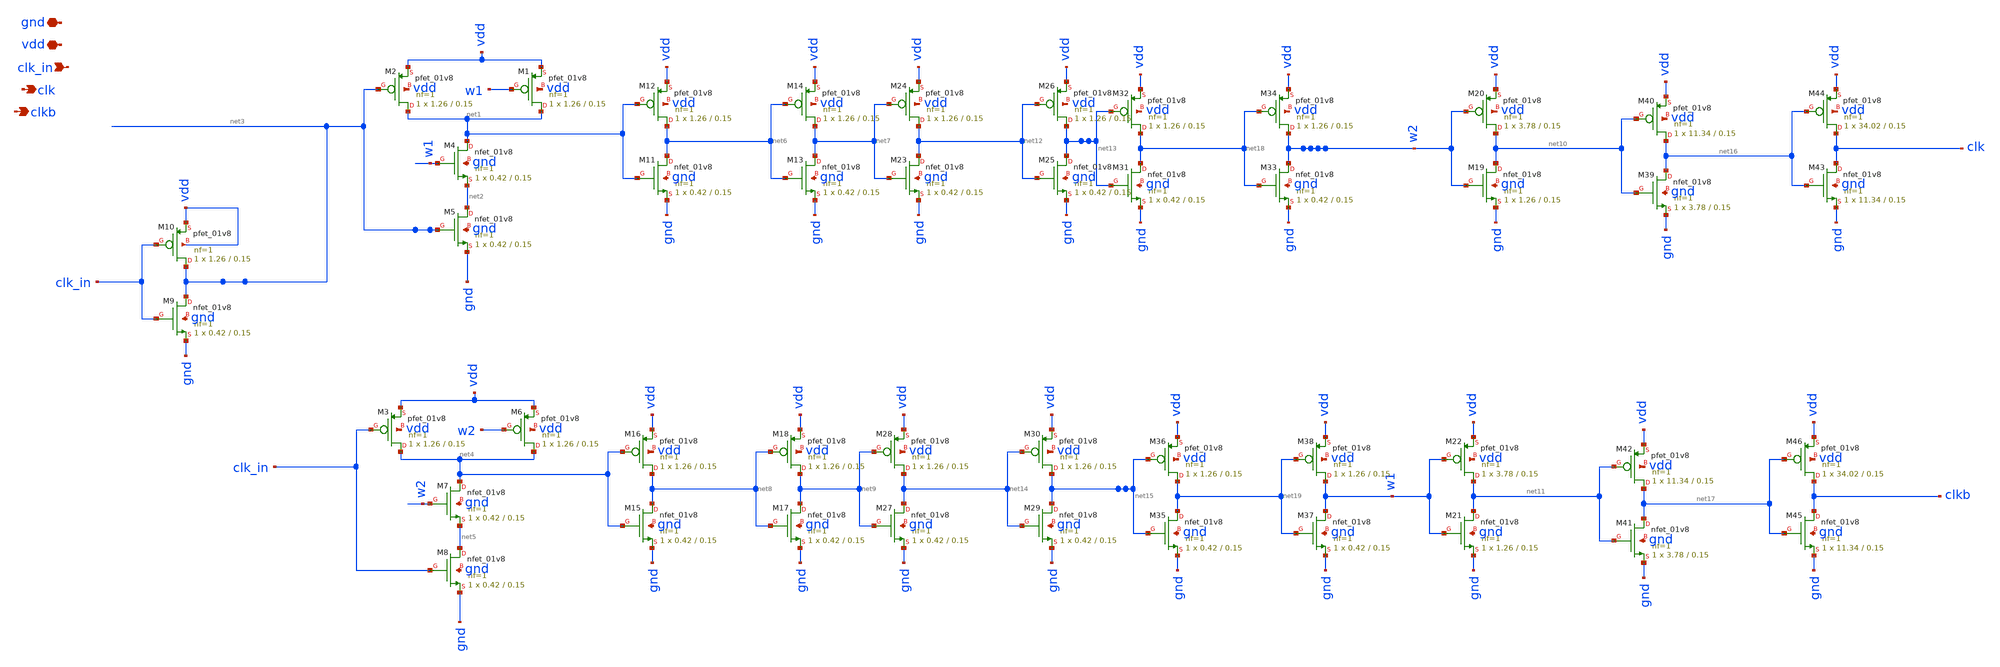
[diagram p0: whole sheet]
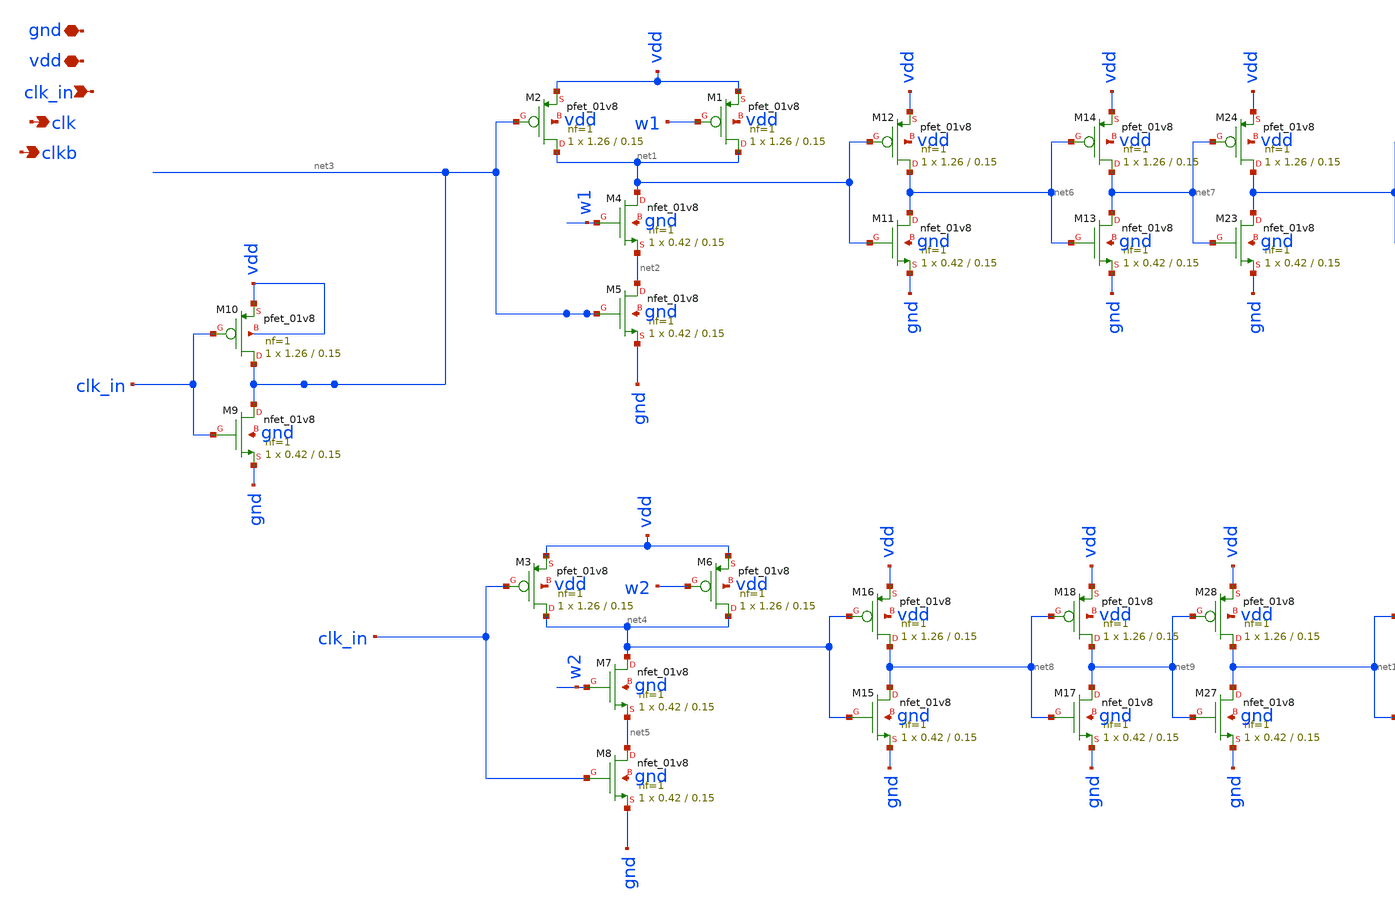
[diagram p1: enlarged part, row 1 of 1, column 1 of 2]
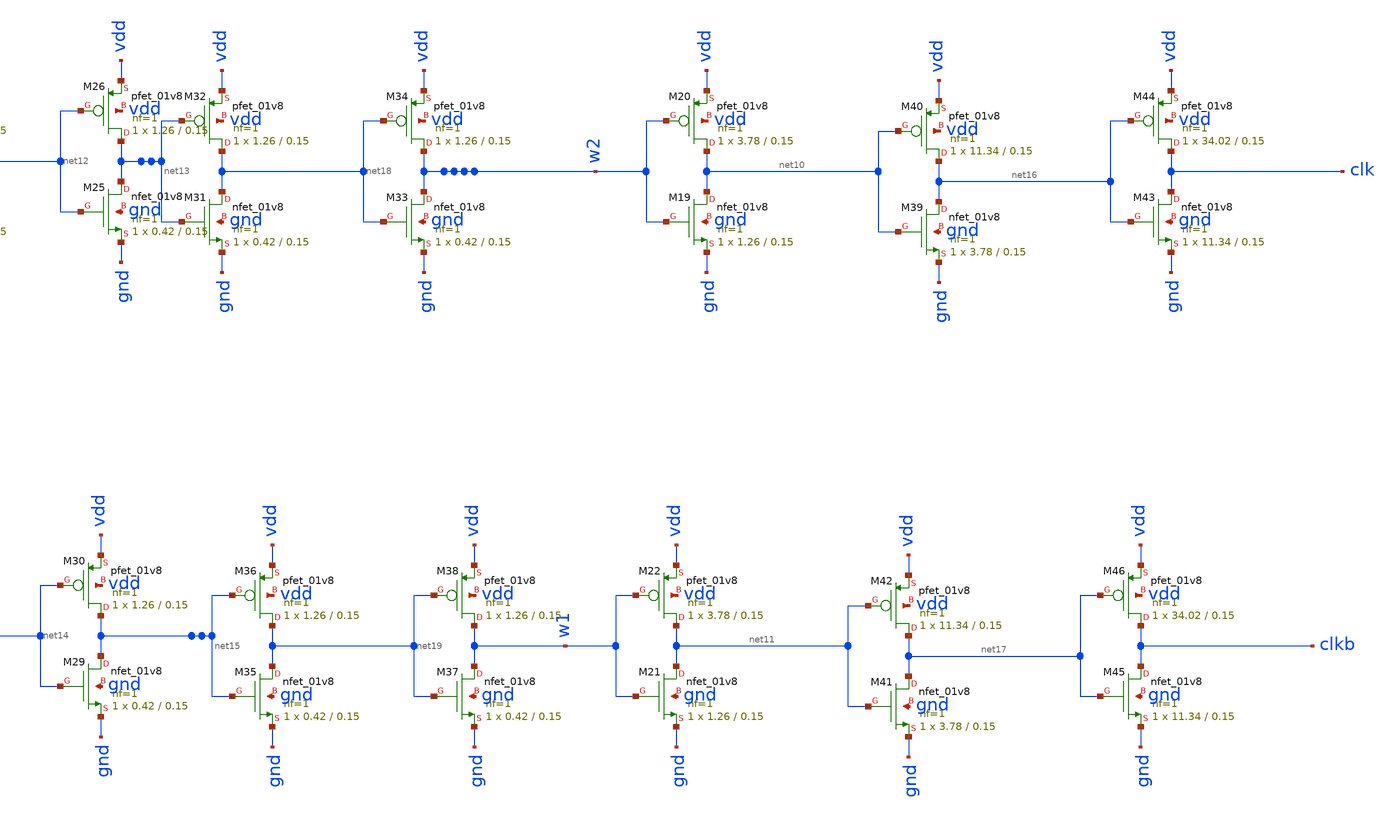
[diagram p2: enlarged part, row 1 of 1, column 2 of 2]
** sch_path: xschem/charge_pumps2/clock_1.sch
**.subckt clock_1 clk_in vdd gnd clk clkb
*.ipin clk_in
*.iopin vdd
*.iopin gnd
*.opin clk
*.opin clkb
XM2 net1 net3 vdd vdd sky130_fd_pr__pfet_01v8 L=0.15 W=1.26 nf=1 ad='int((nf+1)/2) * W/nf * 0.29' as='int((nf+2)/2) * W/nf * 0.29'
+ pd='2*int((nf+1)/2) * (W/nf + 0.29)' ps='2*int((nf+2)/2) * (W/nf + 0.29)' nrd='0.29 / W' nrs='0.29 / W'
+ sa=0 sb=0 sd=0 mult=1 m=1
XM1 net1 w1 vdd vdd sky130_fd_pr__pfet_01v8 L=0.15 W=1.26 nf=1 ad='int((nf+1)/2) * W/nf * 0.29' as='int((nf+2)/2) * W/nf * 0.29'
+ pd='2*int((nf+1)/2) * (W/nf + 0.29)' ps='2*int((nf+2)/2) * (W/nf + 0.29)' nrd='0.29 / W' nrs='0.29 / W'
+ sa=0 sb=0 sd=0 mult=1 m=1
XM4 net1 w1 net2 gnd sky130_fd_pr__nfet_01v8 L=0.15 W=0.42 nf=1 ad='int((nf+1)/2) * W/nf * 0.29' as='int((nf+2)/2) * W/nf * 0.29'
+ pd='2*int((nf+1)/2) * (W/nf + 0.29)' ps='2*int((nf+2)/2) * (W/nf + 0.29)' nrd='0.29 / W' nrs='0.29 / W'
+ sa=0 sb=0 sd=0 mult=1 m=1
XM5 net2 net3 gnd gnd sky130_fd_pr__nfet_01v8 L=0.15 W=0.42 nf=1 ad='int((nf+1)/2) * W/nf * 0.29' as='int((nf+2)/2) * W/nf * 0.29'
+ pd='2*int((nf+1)/2) * (W/nf + 0.29)' ps='2*int((nf+2)/2) * (W/nf + 0.29)' nrd='0.29 / W' nrs='0.29 / W'
+ sa=0 sb=0 sd=0 mult=1 m=1
XM3 net4 clk_in vdd vdd sky130_fd_pr__pfet_01v8 L=0.15 W=1.26 nf=1 ad='int((nf+1)/2) * W/nf * 0.29' as='int((nf+2)/2) * W/nf * 0.29'
+ pd='2*int((nf+1)/2) * (W/nf + 0.29)' ps='2*int((nf+2)/2) * (W/nf + 0.29)' nrd='0.29 / W' nrs='0.29 / W'
+ sa=0 sb=0 sd=0 mult=1 m=1
XM6 net4 w2 vdd vdd sky130_fd_pr__pfet_01v8 L=0.15 W=1.26 nf=1 ad='int((nf+1)/2) * W/nf * 0.29' as='int((nf+2)/2) * W/nf * 0.29'
+ pd='2*int((nf+1)/2) * (W/nf + 0.29)' ps='2*int((nf+2)/2) * (W/nf + 0.29)' nrd='0.29 / W' nrs='0.29 / W'
+ sa=0 sb=0 sd=0 mult=1 m=1
XM7 net4 w2 net5 gnd sky130_fd_pr__nfet_01v8 L=0.15 W=0.42 nf=1 ad='int((nf+1)/2) * W/nf * 0.29' as='int((nf+2)/2) * W/nf * 0.29'
+ pd='2*int((nf+1)/2) * (W/nf + 0.29)' ps='2*int((nf+2)/2) * (W/nf + 0.29)' nrd='0.29 / W' nrs='0.29 / W'
+ sa=0 sb=0 sd=0 mult=1 m=1
XM8 net5 clk_in gnd gnd sky130_fd_pr__nfet_01v8 L=0.15 W=0.42 nf=1 ad='int((nf+1)/2) * W/nf * 0.29' as='int((nf+2)/2) * W/nf * 0.29'
+ pd='2*int((nf+1)/2) * (W/nf + 0.29)' ps='2*int((nf+2)/2) * (W/nf + 0.29)' nrd='0.29 / W' nrs='0.29 / W'
+ sa=0 sb=0 sd=0 mult=1 m=1
XM9 net3 clk_in gnd gnd sky130_fd_pr__nfet_01v8 L=0.15 W=0.42 nf=1 ad='int((nf+1)/2) * W/nf * 0.29' as='int((nf+2)/2) * W/nf * 0.29'
+ pd='2*int((nf+1)/2) * (W/nf + 0.29)' ps='2*int((nf+2)/2) * (W/nf + 0.29)' nrd='0.29 / W' nrs='0.29 / W'
+ sa=0 sb=0 sd=0 mult=1 m=1
XM10 net3 clk_in vdd vdd sky130_fd_pr__pfet_01v8 L=0.15 W=1.26 nf=1 ad='int((nf+1)/2) * W/nf * 0.29'
+ as='int((nf+2)/2) * W/nf * 0.29' pd='2*int((nf+1)/2) * (W/nf + 0.29)' ps='2*int((nf+2)/2) * (W/nf + 0.29)'
+ nrd='0.29 / W' nrs='0.29 / W' sa=0 sb=0 sd=0 mult=1 m=1
XM11 net6 net1 gnd gnd sky130_fd_pr__nfet_01v8 L=0.15 W=0.42 nf=1 ad='int((nf+1)/2) * W/nf * 0.29' as='int((nf+2)/2) * W/nf * 0.29'
+ pd='2*int((nf+1)/2) * (W/nf + 0.29)' ps='2*int((nf+2)/2) * (W/nf + 0.29)' nrd='0.29 / W' nrs='0.29 / W'
+ sa=0 sb=0 sd=0 mult=1 m=1
XM12 net6 net1 vdd vdd sky130_fd_pr__pfet_01v8 L=0.15 W=1.26 nf=1 ad='int((nf+1)/2) * W/nf * 0.29' as='int((nf+2)/2) * W/nf * 0.29'
+ pd='2*int((nf+1)/2) * (W/nf + 0.29)' ps='2*int((nf+2)/2) * (W/nf + 0.29)' nrd='0.29 / W' nrs='0.29 / W'
+ sa=0 sb=0 sd=0 mult=1 m=1
XM13 net7 net6 gnd gnd sky130_fd_pr__nfet_01v8 L=0.15 W=0.42 nf=1 ad='int((nf+1)/2) * W/nf * 0.29' as='int((nf+2)/2) * W/nf * 0.29'
+ pd='2*int((nf+1)/2) * (W/nf + 0.29)' ps='2*int((nf+2)/2) * (W/nf + 0.29)' nrd='0.29 / W' nrs='0.29 / W'
+ sa=0 sb=0 sd=0 mult=1 m=1
XM14 net7 net6 vdd vdd sky130_fd_pr__pfet_01v8 L=0.15 W=1.26 nf=1 ad='int((nf+1)/2) * W/nf * 0.29' as='int((nf+2)/2) * W/nf * 0.29'
+ pd='2*int((nf+1)/2) * (W/nf + 0.29)' ps='2*int((nf+2)/2) * (W/nf + 0.29)' nrd='0.29 / W' nrs='0.29 / W'
+ sa=0 sb=0 sd=0 mult=1 m=1
XM15 net8 net4 gnd gnd sky130_fd_pr__nfet_01v8 L=0.15 W=0.42 nf=1 ad='int((nf+1)/2) * W/nf * 0.29' as='int((nf+2)/2) * W/nf * 0.29'
+ pd='2*int((nf+1)/2) * (W/nf + 0.29)' ps='2*int((nf+2)/2) * (W/nf + 0.29)' nrd='0.29 / W' nrs='0.29 / W'
+ sa=0 sb=0 sd=0 mult=1 m=1
XM16 net8 net4 vdd vdd sky130_fd_pr__pfet_01v8 L=0.15 W=1.26 nf=1 ad='int((nf+1)/2) * W/nf * 0.29' as='int((nf+2)/2) * W/nf * 0.29'
+ pd='2*int((nf+1)/2) * (W/nf + 0.29)' ps='2*int((nf+2)/2) * (W/nf + 0.29)' nrd='0.29 / W' nrs='0.29 / W'
+ sa=0 sb=0 sd=0 mult=1 m=1
XM17 net9 net8 gnd gnd sky130_fd_pr__nfet_01v8 L=0.15 W=0.42 nf=1 ad='int((nf+1)/2) * W/nf * 0.29' as='int((nf+2)/2) * W/nf * 0.29'
+ pd='2*int((nf+1)/2) * (W/nf + 0.29)' ps='2*int((nf+2)/2) * (W/nf + 0.29)' nrd='0.29 / W' nrs='0.29 / W'
+ sa=0 sb=0 sd=0 mult=1 m=1
XM18 net9 net8 vdd vdd sky130_fd_pr__pfet_01v8 L=0.15 W=1.26 nf=1 ad='int((nf+1)/2) * W/nf * 0.29' as='int((nf+2)/2) * W/nf * 0.29'
+ pd='2*int((nf+1)/2) * (W/nf + 0.29)' ps='2*int((nf+2)/2) * (W/nf + 0.29)' nrd='0.29 / W' nrs='0.29 / W'
+ sa=0 sb=0 sd=0 mult=1 m=1
XM19 net10 w2 gnd gnd sky130_fd_pr__nfet_01v8 L=0.15 W=1.26 nf=1 ad='int((nf+1)/2) * W/nf * 0.29' as='int((nf+2)/2) * W/nf * 0.29'
+ pd='2*int((nf+1)/2) * (W/nf + 0.29)' ps='2*int((nf+2)/2) * (W/nf + 0.29)' nrd='0.29 / W' nrs='0.29 / W'
+ sa=0 sb=0 sd=0 mult=1 m=1
XM20 net10 w2 vdd vdd sky130_fd_pr__pfet_01v8 L=0.15 W=3.78 nf=1 ad='int((nf+1)/2) * W/nf * 0.29' as='int((nf+2)/2) * W/nf * 0.29'
+ pd='2*int((nf+1)/2) * (W/nf + 0.29)' ps='2*int((nf+2)/2) * (W/nf + 0.29)' nrd='0.29 / W' nrs='0.29 / W'
+ sa=0 sb=0 sd=0 mult=1 m=1
XM21 net11 w1 gnd gnd sky130_fd_pr__nfet_01v8 L=0.15 W=1.26 nf=1 ad='int((nf+1)/2) * W/nf * 0.29' as='int((nf+2)/2) * W/nf * 0.29'
+ pd='2*int((nf+1)/2) * (W/nf + 0.29)' ps='2*int((nf+2)/2) * (W/nf + 0.29)' nrd='0.29 / W' nrs='0.29 / W'
+ sa=0 sb=0 sd=0 mult=1 m=1
XM22 net11 w1 vdd vdd sky130_fd_pr__pfet_01v8 L=0.15 W=3.78 nf=1 ad='int((nf+1)/2) * W/nf * 0.29' as='int((nf+2)/2) * W/nf * 0.29'
+ pd='2*int((nf+1)/2) * (W/nf + 0.29)' ps='2*int((nf+2)/2) * (W/nf + 0.29)' nrd='0.29 / W' nrs='0.29 / W'
+ sa=0 sb=0 sd=0 mult=1 m=1
XM23 net12 net7 gnd gnd sky130_fd_pr__nfet_01v8 L=0.15 W=0.42 nf=1 ad='int((nf+1)/2) * W/nf * 0.29' as='int((nf+2)/2) * W/nf * 0.29'
+ pd='2*int((nf+1)/2) * (W/nf + 0.29)' ps='2*int((nf+2)/2) * (W/nf + 0.29)' nrd='0.29 / W' nrs='0.29 / W'
+ sa=0 sb=0 sd=0 mult=1 m=1
XM24 net12 net7 vdd vdd sky130_fd_pr__pfet_01v8 L=0.15 W=1.26 nf=1 ad='int((nf+1)/2) * W/nf * 0.29' as='int((nf+2)/2) * W/nf * 0.29'
+ pd='2*int((nf+1)/2) * (W/nf + 0.29)' ps='2*int((nf+2)/2) * (W/nf + 0.29)' nrd='0.29 / W' nrs='0.29 / W'
+ sa=0 sb=0 sd=0 mult=1 m=1
XM25 net13 net12 gnd gnd sky130_fd_pr__nfet_01v8 L=0.15 W=0.42 nf=1 ad='int((nf+1)/2) * W/nf * 0.29'
+ as='int((nf+2)/2) * W/nf * 0.29' pd='2*int((nf+1)/2) * (W/nf + 0.29)' ps='2*int((nf+2)/2) * (W/nf + 0.29)'
+ nrd='0.29 / W' nrs='0.29 / W' sa=0 sb=0 sd=0 mult=1 m=1
XM26 net13 net12 vdd vdd sky130_fd_pr__pfet_01v8 L=0.15 W=1.26 nf=1 ad='int((nf+1)/2) * W/nf * 0.29'
+ as='int((nf+2)/2) * W/nf * 0.29' pd='2*int((nf+1)/2) * (W/nf + 0.29)' ps='2*int((nf+2)/2) * (W/nf + 0.29)'
+ nrd='0.29 / W' nrs='0.29 / W' sa=0 sb=0 sd=0 mult=1 m=1
XM27 net14 net9 gnd gnd sky130_fd_pr__nfet_01v8 L=0.15 W=0.42 nf=1 ad='int((nf+1)/2) * W/nf * 0.29' as='int((nf+2)/2) * W/nf * 0.29'
+ pd='2*int((nf+1)/2) * (W/nf + 0.29)' ps='2*int((nf+2)/2) * (W/nf + 0.29)' nrd='0.29 / W' nrs='0.29 / W'
+ sa=0 sb=0 sd=0 mult=1 m=1
XM28 net14 net9 vdd vdd sky130_fd_pr__pfet_01v8 L=0.15 W=1.26 nf=1 ad='int((nf+1)/2) * W/nf * 0.29' as='int((nf+2)/2) * W/nf * 0.29'
+ pd='2*int((nf+1)/2) * (W/nf + 0.29)' ps='2*int((nf+2)/2) * (W/nf + 0.29)' nrd='0.29 / W' nrs='0.29 / W'
+ sa=0 sb=0 sd=0 mult=1 m=1
XM29 net15 net14 gnd gnd sky130_fd_pr__nfet_01v8 L=0.15 W=0.42 nf=1 ad='int((nf+1)/2) * W/nf * 0.29'
+ as='int((nf+2)/2) * W/nf * 0.29' pd='2*int((nf+1)/2) * (W/nf + 0.29)' ps='2*int((nf+2)/2) * (W/nf + 0.29)'
+ nrd='0.29 / W' nrs='0.29 / W' sa=0 sb=0 sd=0 mult=1 m=1
XM30 net15 net14 vdd vdd sky130_fd_pr__pfet_01v8 L=0.15 W=1.26 nf=1 ad='int((nf+1)/2) * W/nf * 0.29'
+ as='int((nf+2)/2) * W/nf * 0.29' pd='2*int((nf+1)/2) * (W/nf + 0.29)' ps='2*int((nf+2)/2) * (W/nf + 0.29)'
+ nrd='0.29 / W' nrs='0.29 / W' sa=0 sb=0 sd=0 mult=1 m=1
XM39 net16 net10 gnd gnd sky130_fd_pr__nfet_01v8 L=0.15 W=3.78 nf=1 ad='int((nf+1)/2) * W/nf * 0.29'
+ as='int((nf+2)/2) * W/nf * 0.29' pd='2*int((nf+1)/2) * (W/nf + 0.29)' ps='2*int((nf+2)/2) * (W/nf + 0.29)'
+ nrd='0.29 / W' nrs='0.29 / W' sa=0 sb=0 sd=0 mult=1 m=1
XM40 net16 net10 vdd vdd sky130_fd_pr__pfet_01v8 L=0.15 W=11.34 nf=1 ad='int((nf+1)/2) * W/nf * 0.29'
+ as='int((nf+2)/2) * W/nf * 0.29' pd='2*int((nf+1)/2) * (W/nf + 0.29)' ps='2*int((nf+2)/2) * (W/nf + 0.29)'
+ nrd='0.29 / W' nrs='0.29 / W' sa=0 sb=0 sd=0 mult=1 m=1
XM41 net17 net11 gnd gnd sky130_fd_pr__nfet_01v8 L=0.15 W=3.78 nf=1 ad='int((nf+1)/2) * W/nf * 0.29'
+ as='int((nf+2)/2) * W/nf * 0.29' pd='2*int((nf+1)/2) * (W/nf + 0.29)' ps='2*int((nf+2)/2) * (W/nf + 0.29)'
+ nrd='0.29 / W' nrs='0.29 / W' sa=0 sb=0 sd=0 mult=1 m=1
XM42 net17 net11 vdd vdd sky130_fd_pr__pfet_01v8 L=0.15 W=11.34 nf=1 ad='int((nf+1)/2) * W/nf * 0.29'
+ as='int((nf+2)/2) * W/nf * 0.29' pd='2*int((nf+1)/2) * (W/nf + 0.29)' ps='2*int((nf+2)/2) * (W/nf + 0.29)'
+ nrd='0.29 / W' nrs='0.29 / W' sa=0 sb=0 sd=0 mult=1 m=1
XM43 clk net16 gnd gnd sky130_fd_pr__nfet_01v8 L=0.15 W=11.34 nf=1 ad='int((nf+1)/2) * W/nf * 0.29' as='int((nf+2)/2) * W/nf * 0.29'
+ pd='2*int((nf+1)/2) * (W/nf + 0.29)' ps='2*int((nf+2)/2) * (W/nf + 0.29)' nrd='0.29 / W' nrs='0.29 / W'
+ sa=0 sb=0 sd=0 mult=1 m=1
XM44 clk net16 vdd vdd sky130_fd_pr__pfet_01v8 L=0.15 W=34.02 nf=1 ad='int((nf+1)/2) * W/nf * 0.29' as='int((nf+2)/2) * W/nf * 0.29'
+ pd='2*int((nf+1)/2) * (W/nf + 0.29)' ps='2*int((nf+2)/2) * (W/nf + 0.29)' nrd='0.29 / W' nrs='0.29 / W'
+ sa=0 sb=0 sd=0 mult=1 m=1
XM45 clkb net17 gnd gnd sky130_fd_pr__nfet_01v8 L=0.15 W=11.34 nf=1 ad='int((nf+1)/2) * W/nf * 0.29'
+ as='int((nf+2)/2) * W/nf * 0.29' pd='2*int((nf+1)/2) * (W/nf + 0.29)' ps='2*int((nf+2)/2) * (W/nf + 0.29)'
+ nrd='0.29 / W' nrs='0.29 / W' sa=0 sb=0 sd=0 mult=1 m=1
XM46 clkb net17 vdd vdd sky130_fd_pr__pfet_01v8 L=0.15 W=34.02 nf=1 ad='int((nf+1)/2) * W/nf * 0.29'
+ as='int((nf+2)/2) * W/nf * 0.29' pd='2*int((nf+1)/2) * (W/nf + 0.29)' ps='2*int((nf+2)/2) * (W/nf + 0.29)'
+ nrd='0.29 / W' nrs='0.29 / W' sa=0 sb=0 sd=0 mult=1 m=1
XM31 net18 net13 gnd gnd sky130_fd_pr__nfet_01v8 L=0.15 W=0.42 nf=1 ad='int((nf+1)/2) * W/nf * 0.29'
+ as='int((nf+2)/2) * W/nf * 0.29' pd='2*int((nf+1)/2) * (W/nf + 0.29)' ps='2*int((nf+2)/2) * (W/nf + 0.29)'
+ nrd='0.29 / W' nrs='0.29 / W' sa=0 sb=0 sd=0 mult=1 m=1
XM32 net18 net13 vdd vdd sky130_fd_pr__pfet_01v8 L=0.15 W=1.26 nf=1 ad='int((nf+1)/2) * W/nf * 0.29'
+ as='int((nf+2)/2) * W/nf * 0.29' pd='2*int((nf+1)/2) * (W/nf + 0.29)' ps='2*int((nf+2)/2) * (W/nf + 0.29)'
+ nrd='0.29 / W' nrs='0.29 / W' sa=0 sb=0 sd=0 mult=1 m=1
XM33 w2 net18 gnd gnd sky130_fd_pr__nfet_01v8 L=0.15 W=0.42 nf=1 ad='int((nf+1)/2) * W/nf * 0.29' as='int((nf+2)/2) * W/nf * 0.29'
+ pd='2*int((nf+1)/2) * (W/nf + 0.29)' ps='2*int((nf+2)/2) * (W/nf + 0.29)' nrd='0.29 / W' nrs='0.29 / W'
+ sa=0 sb=0 sd=0 mult=1 m=1
XM34 w2 net18 vdd vdd sky130_fd_pr__pfet_01v8 L=0.15 W=1.26 nf=1 ad='int((nf+1)/2) * W/nf * 0.29' as='int((nf+2)/2) * W/nf * 0.29'
+ pd='2*int((nf+1)/2) * (W/nf + 0.29)' ps='2*int((nf+2)/2) * (W/nf + 0.29)' nrd='0.29 / W' nrs='0.29 / W'
+ sa=0 sb=0 sd=0 mult=1 m=1
XM35 net19 net15 gnd gnd sky130_fd_pr__nfet_01v8 L=0.15 W=0.42 nf=1 ad='int((nf+1)/2) * W/nf * 0.29'
+ as='int((nf+2)/2) * W/nf * 0.29' pd='2*int((nf+1)/2) * (W/nf + 0.29)' ps='2*int((nf+2)/2) * (W/nf + 0.29)'
+ nrd='0.29 / W' nrs='0.29 / W' sa=0 sb=0 sd=0 mult=1 m=1
XM36 net19 net15 vdd vdd sky130_fd_pr__pfet_01v8 L=0.15 W=1.26 nf=1 ad='int((nf+1)/2) * W/nf * 0.29'
+ as='int((nf+2)/2) * W/nf * 0.29' pd='2*int((nf+1)/2) * (W/nf + 0.29)' ps='2*int((nf+2)/2) * (W/nf + 0.29)'
+ nrd='0.29 / W' nrs='0.29 / W' sa=0 sb=0 sd=0 mult=1 m=1
XM37 w1 net19 gnd gnd sky130_fd_pr__nfet_01v8 L=0.15 W=0.42 nf=1 ad='int((nf+1)/2) * W/nf * 0.29' as='int((nf+2)/2) * W/nf * 0.29'
+ pd='2*int((nf+1)/2) * (W/nf + 0.29)' ps='2*int((nf+2)/2) * (W/nf + 0.29)' nrd='0.29 / W' nrs='0.29 / W'
+ sa=0 sb=0 sd=0 mult=1 m=1
XM38 w1 net19 vdd vdd sky130_fd_pr__pfet_01v8 L=0.15 W=1.26 nf=1 ad='int((nf+1)/2) * W/nf * 0.29' as='int((nf+2)/2) * W/nf * 0.29'
+ pd='2*int((nf+1)/2) * (W/nf + 0.29)' ps='2*int((nf+2)/2) * (W/nf + 0.29)' nrd='0.29 / W' nrs='0.29 / W'
+ sa=0 sb=0 sd=0 mult=1 m=1
**.ends
.end
